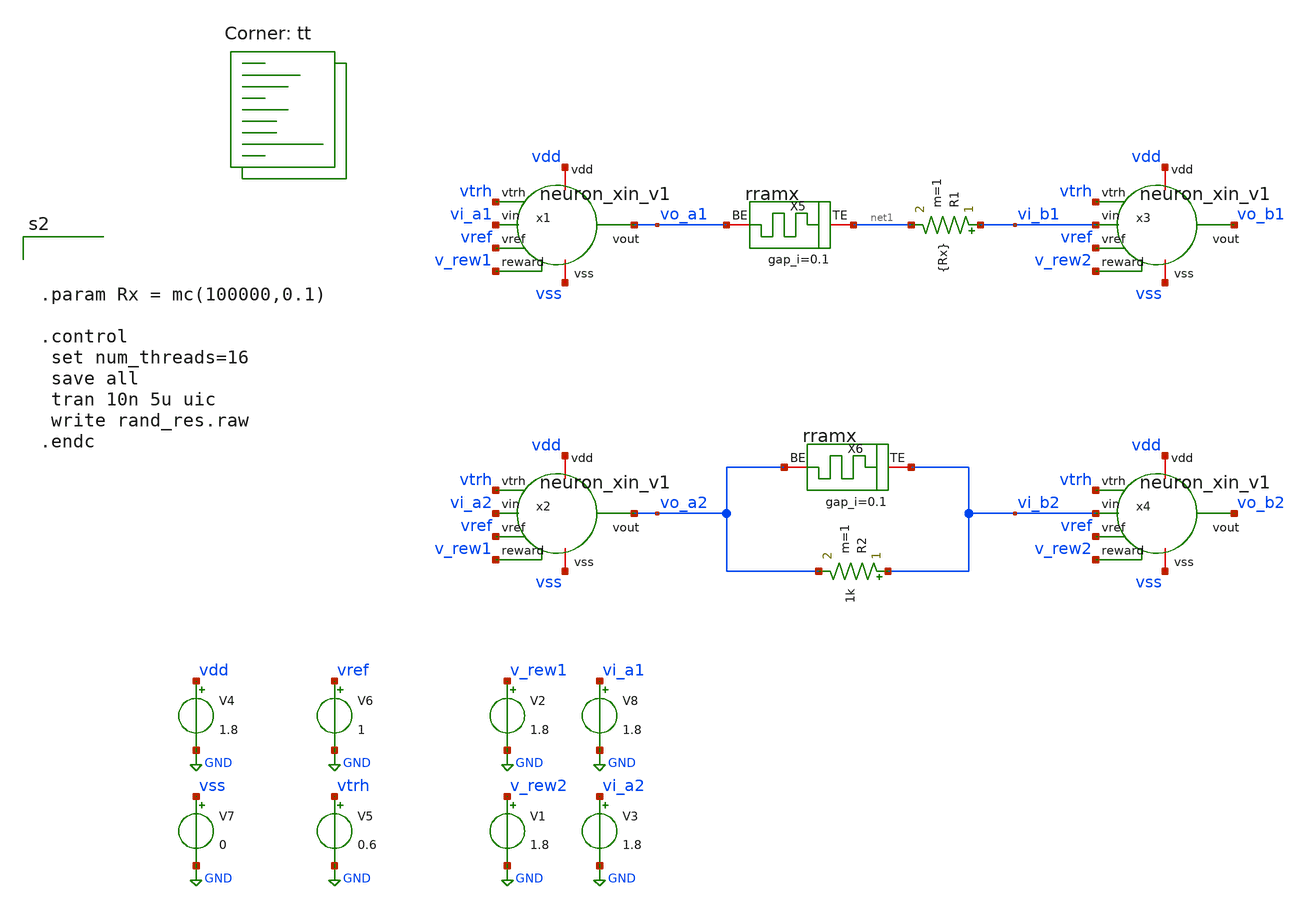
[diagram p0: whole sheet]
** sch_path: tests/rand_res.sch
**.subckt rand_res
V4 vdd GND 1.8
V5 vtrh GND 0.6
V6 vref GND 1
V7 vss GND 0
x1 vdd vss vo_a1 vi_a1 vtrh vref v_rew1 neuron_xin_v1
x2 vdd vss vo_a2 vi_a2 vtrh vref v_rew1 neuron_xin_v1
x3 vdd vss vo_b1 vi_b1 vtrh vref v_rew2 neuron_xin_v1
x4 vdd vss vo_b2 vi_b2 vtrh vref v_rew2 neuron_xin_v1
X5 net1 vo_a1 rram_cell gap_i=0.1
X6 vi_b2 vo_a2 rram_cell gap_i=0.1
R1 vi_b1 net1 {Rx} m=1
R2 vi_b2 vo_a2 1k m=1
V1 v_rew2 GND 1.8
V2 v_rew1 GND 1.8
V3 vi_a2 GND 1.8
V8 vi_a1 GND 1.8
**** begin user architecture code



.param Rx = mc(100000,0.1)

.control
 set num_threads=16
 save all
 tran 10n 5u uic
 write rand_res.raw
.endc



.lib $::SKYWATER_MODELS/sky130.lib.spice tt

.subckt rram_cell BE TE gap_i=0.1
N1 BE TE rram_model
.model rram_model rram gap_initial={gap_i}
.ends rram_cell

.control
pre_osdi /foss/designs/spike_130/designs/prubs/rram.osdi
.endc

**** end user architecture code
**.ends
.GLOBAL GND
.end
